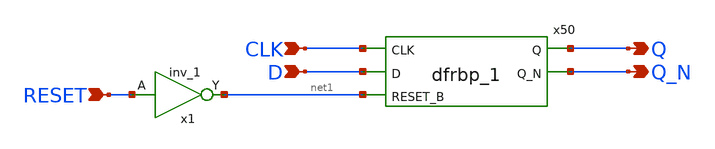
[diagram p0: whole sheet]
** sch_path: xschem/adc/mydf.sch
**.subckt mydf CLK D RESET Q Q_N
*.ipin CLK
*.ipin D
*.ipin RESET
*.opin Q
*.opin Q_N
x50 CLK D net1 dvss dvss dvdd dvdd Q Q_N sky130_fd_sc_hd__dfrbp_1
x1 RESET dvss dvss dvdd dvdd net1 sky130_fd_sc_hd__inv_1
**.ends
.end
